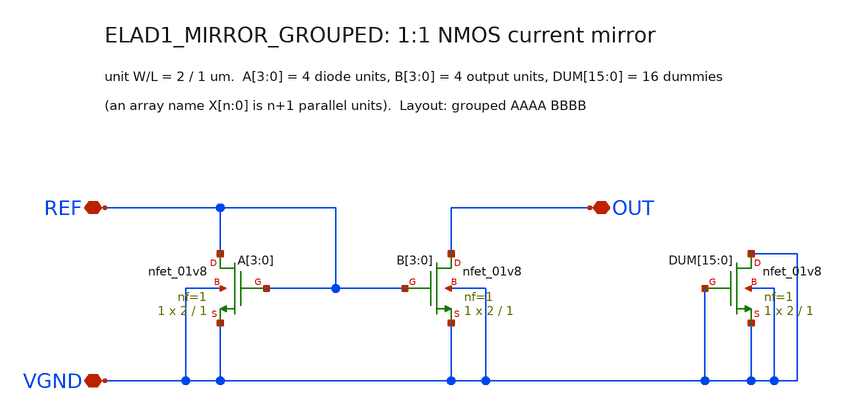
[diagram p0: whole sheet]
** sch_path: cells/ELAD1_MIRROR_GROUPED/schematic/ELAD1_MIRROR_GROUPED.sch
**.subckt ELAD1_MIRROR_GROUPED REF OUT VGND
*.iopin REF
*.iopin OUT
*.iopin VGND
XA[3] REF REF VGND VGND sky130_fd_pr__nfet_01v8 L=1 W=2 nf=1 ad='int((1 + 1)/2) * 2 / 1 * 0.29' as='int((1 + 2)/2) * 2 / 1 * 0.29'
+ pd='2*int((1 + 1)/2) * (2 / 1 + 0.29)' ps='2*int((1 + 2)/2) * (2 / 1 + 0.29)' nrd='0.29 / 2 ' nrs='0.29 / 2 '
+ sa=0 sb=0 sd=0 mult=1 m=1
XA[2] REF REF VGND VGND sky130_fd_pr__nfet_01v8 L=1 W=2 nf=1 ad='int((1 + 1)/2) * 2 / 1 * 0.29' as='int((1 + 2)/2) * 2 / 1 * 0.29'
+ pd='2*int((1 + 1)/2) * (2 / 1 + 0.29)' ps='2*int((1 + 2)/2) * (2 / 1 + 0.29)' nrd='0.29 / 2 ' nrs='0.29 / 2 '
+ sa=0 sb=0 sd=0 mult=1 m=1
XA[1] REF REF VGND VGND sky130_fd_pr__nfet_01v8 L=1 W=2 nf=1 ad='int((1 + 1)/2) * 2 / 1 * 0.29' as='int((1 + 2)/2) * 2 / 1 * 0.29'
+ pd='2*int((1 + 1)/2) * (2 / 1 + 0.29)' ps='2*int((1 + 2)/2) * (2 / 1 + 0.29)' nrd='0.29 / 2 ' nrs='0.29 / 2 '
+ sa=0 sb=0 sd=0 mult=1 m=1
XA[0] REF REF VGND VGND sky130_fd_pr__nfet_01v8 L=1 W=2 nf=1 ad='int((1 + 1)/2) * 2 / 1 * 0.29' as='int((1 + 2)/2) * 2 / 1 * 0.29'
+ pd='2*int((1 + 1)/2) * (2 / 1 + 0.29)' ps='2*int((1 + 2)/2) * (2 / 1 + 0.29)' nrd='0.29 / 2 ' nrs='0.29 / 2 '
+ sa=0 sb=0 sd=0 mult=1 m=1
XB[3] OUT REF VGND VGND sky130_fd_pr__nfet_01v8 L=1 W=2 nf=1 ad='int((1 + 1)/2) * 2 / 1 * 0.29' as='int((1 + 2)/2) * 2 / 1 * 0.29'
+ pd='2*int((1 + 1)/2) * (2 / 1 + 0.29)' ps='2*int((1 + 2)/2) * (2 / 1 + 0.29)' nrd='0.29 / 2 ' nrs='0.29 / 2 '
+ sa=0 sb=0 sd=0 mult=1 m=1
XB[2] OUT REF VGND VGND sky130_fd_pr__nfet_01v8 L=1 W=2 nf=1 ad='int((1 + 1)/2) * 2 / 1 * 0.29' as='int((1 + 2)/2) * 2 / 1 * 0.29'
+ pd='2*int((1 + 1)/2) * (2 / 1 + 0.29)' ps='2*int((1 + 2)/2) * (2 / 1 + 0.29)' nrd='0.29 / 2 ' nrs='0.29 / 2 '
+ sa=0 sb=0 sd=0 mult=1 m=1
XB[1] OUT REF VGND VGND sky130_fd_pr__nfet_01v8 L=1 W=2 nf=1 ad='int((1 + 1)/2) * 2 / 1 * 0.29' as='int((1 + 2)/2) * 2 / 1 * 0.29'
+ pd='2*int((1 + 1)/2) * (2 / 1 + 0.29)' ps='2*int((1 + 2)/2) * (2 / 1 + 0.29)' nrd='0.29 / 2 ' nrs='0.29 / 2 '
+ sa=0 sb=0 sd=0 mult=1 m=1
XB[0] OUT REF VGND VGND sky130_fd_pr__nfet_01v8 L=1 W=2 nf=1 ad='int((1 + 1)/2) * 2 / 1 * 0.29' as='int((1 + 2)/2) * 2 / 1 * 0.29'
+ pd='2*int((1 + 1)/2) * (2 / 1 + 0.29)' ps='2*int((1 + 2)/2) * (2 / 1 + 0.29)' nrd='0.29 / 2 ' nrs='0.29 / 2 '
+ sa=0 sb=0 sd=0 mult=1 m=1
XDUM[15] VGND VGND VGND VGND sky130_fd_pr__nfet_01v8 L=1 W=2 nf=1 ad='int((1 + 1)/2) * 2 / 1 * 0.29'
+ as='int((1 + 2)/2) * 2 / 1 * 0.29' pd='2*int((1 + 1)/2) * (2 / 1 + 0.29)' ps='2*int((1 + 2)/2) * (2 / 1 + 0.29)'
+ nrd='0.29 / 2 ' nrs='0.29 / 2 ' sa=0 sb=0 sd=0 mult=1 m=1
XDUM[14] VGND VGND VGND VGND sky130_fd_pr__nfet_01v8 L=1 W=2 nf=1 ad='int((1 + 1)/2) * 2 / 1 * 0.29'
+ as='int((1 + 2)/2) * 2 / 1 * 0.29' pd='2*int((1 + 1)/2) * (2 / 1 + 0.29)' ps='2*int((1 + 2)/2) * (2 / 1 + 0.29)'
+ nrd='0.29 / 2 ' nrs='0.29 / 2 ' sa=0 sb=0 sd=0 mult=1 m=1
XDUM[13] VGND VGND VGND VGND sky130_fd_pr__nfet_01v8 L=1 W=2 nf=1 ad='int((1 + 1)/2) * 2 / 1 * 0.29'
+ as='int((1 + 2)/2) * 2 / 1 * 0.29' pd='2*int((1 + 1)/2) * (2 / 1 + 0.29)' ps='2*int((1 + 2)/2) * (2 / 1 + 0.29)'
+ nrd='0.29 / 2 ' nrs='0.29 / 2 ' sa=0 sb=0 sd=0 mult=1 m=1
XDUM[12] VGND VGND VGND VGND sky130_fd_pr__nfet_01v8 L=1 W=2 nf=1 ad='int((1 + 1)/2) * 2 / 1 * 0.29'
+ as='int((1 + 2)/2) * 2 / 1 * 0.29' pd='2*int((1 + 1)/2) * (2 / 1 + 0.29)' ps='2*int((1 + 2)/2) * (2 / 1 + 0.29)'
+ nrd='0.29 / 2 ' nrs='0.29 / 2 ' sa=0 sb=0 sd=0 mult=1 m=1
XDUM[11] VGND VGND VGND VGND sky130_fd_pr__nfet_01v8 L=1 W=2 nf=1 ad='int((1 + 1)/2) * 2 / 1 * 0.29'
+ as='int((1 + 2)/2) * 2 / 1 * 0.29' pd='2*int((1 + 1)/2) * (2 / 1 + 0.29)' ps='2*int((1 + 2)/2) * (2 / 1 + 0.29)'
+ nrd='0.29 / 2 ' nrs='0.29 / 2 ' sa=0 sb=0 sd=0 mult=1 m=1
XDUM[10] VGND VGND VGND VGND sky130_fd_pr__nfet_01v8 L=1 W=2 nf=1 ad='int((1 + 1)/2) * 2 / 1 * 0.29'
+ as='int((1 + 2)/2) * 2 / 1 * 0.29' pd='2*int((1 + 1)/2) * (2 / 1 + 0.29)' ps='2*int((1 + 2)/2) * (2 / 1 + 0.29)'
+ nrd='0.29 / 2 ' nrs='0.29 / 2 ' sa=0 sb=0 sd=0 mult=1 m=1
XDUM[9] VGND VGND VGND VGND sky130_fd_pr__nfet_01v8 L=1 W=2 nf=1 ad='int((1 + 1)/2) * 2 / 1 * 0.29' as='int((1 + 2)/2) * 2 / 1 * 0.29'
+ pd='2*int((1 + 1)/2) * (2 / 1 + 0.29)' ps='2*int((1 + 2)/2) * (2 / 1 + 0.29)' nrd='0.29 / 2 ' nrs='0.29 / 2 '
+ sa=0 sb=0 sd=0 mult=1 m=1
XDUM[8] VGND VGND VGND VGND sky130_fd_pr__nfet_01v8 L=1 W=2 nf=1 ad='int((1 + 1)/2) * 2 / 1 * 0.29' as='int((1 + 2)/2) * 2 / 1 * 0.29'
+ pd='2*int((1 + 1)/2) * (2 / 1 + 0.29)' ps='2*int((1 + 2)/2) * (2 / 1 + 0.29)' nrd='0.29 / 2 ' nrs='0.29 / 2 '
+ sa=0 sb=0 sd=0 mult=1 m=1
XDUM[7] VGND VGND VGND VGND sky130_fd_pr__nfet_01v8 L=1 W=2 nf=1 ad='int((1 + 1)/2) * 2 / 1 * 0.29' as='int((1 + 2)/2) * 2 / 1 * 0.29'
+ pd='2*int((1 + 1)/2) * (2 / 1 + 0.29)' ps='2*int((1 + 2)/2) * (2 / 1 + 0.29)' nrd='0.29 / 2 ' nrs='0.29 / 2 '
+ sa=0 sb=0 sd=0 mult=1 m=1
XDUM[6] VGND VGND VGND VGND sky130_fd_pr__nfet_01v8 L=1 W=2 nf=1 ad='int((1 + 1)/2) * 2 / 1 * 0.29' as='int((1 + 2)/2) * 2 / 1 * 0.29'
+ pd='2*int((1 + 1)/2) * (2 / 1 + 0.29)' ps='2*int((1 + 2)/2) * (2 / 1 + 0.29)' nrd='0.29 / 2 ' nrs='0.29 / 2 '
+ sa=0 sb=0 sd=0 mult=1 m=1
XDUM[5] VGND VGND VGND VGND sky130_fd_pr__nfet_01v8 L=1 W=2 nf=1 ad='int((1 + 1)/2) * 2 / 1 * 0.29' as='int((1 + 2)/2) * 2 / 1 * 0.29'
+ pd='2*int((1 + 1)/2) * (2 / 1 + 0.29)' ps='2*int((1 + 2)/2) * (2 / 1 + 0.29)' nrd='0.29 / 2 ' nrs='0.29 / 2 '
+ sa=0 sb=0 sd=0 mult=1 m=1
XDUM[4] VGND VGND VGND VGND sky130_fd_pr__nfet_01v8 L=1 W=2 nf=1 ad='int((1 + 1)/2) * 2 / 1 * 0.29' as='int((1 + 2)/2) * 2 / 1 * 0.29'
+ pd='2*int((1 + 1)/2) * (2 / 1 + 0.29)' ps='2*int((1 + 2)/2) * (2 / 1 + 0.29)' nrd='0.29 / 2 ' nrs='0.29 / 2 '
+ sa=0 sb=0 sd=0 mult=1 m=1
XDUM[3] VGND VGND VGND VGND sky130_fd_pr__nfet_01v8 L=1 W=2 nf=1 ad='int((1 + 1)/2) * 2 / 1 * 0.29' as='int((1 + 2)/2) * 2 / 1 * 0.29'
+ pd='2*int((1 + 1)/2) * (2 / 1 + 0.29)' ps='2*int((1 + 2)/2) * (2 / 1 + 0.29)' nrd='0.29 / 2 ' nrs='0.29 / 2 '
+ sa=0 sb=0 sd=0 mult=1 m=1
XDUM[2] VGND VGND VGND VGND sky130_fd_pr__nfet_01v8 L=1 W=2 nf=1 ad='int((1 + 1)/2) * 2 / 1 * 0.29' as='int((1 + 2)/2) * 2 / 1 * 0.29'
+ pd='2*int((1 + 1)/2) * (2 / 1 + 0.29)' ps='2*int((1 + 2)/2) * (2 / 1 + 0.29)' nrd='0.29 / 2 ' nrs='0.29 / 2 '
+ sa=0 sb=0 sd=0 mult=1 m=1
XDUM[1] VGND VGND VGND VGND sky130_fd_pr__nfet_01v8 L=1 W=2 nf=1 ad='int((1 + 1)/2) * 2 / 1 * 0.29' as='int((1 + 2)/2) * 2 / 1 * 0.29'
+ pd='2*int((1 + 1)/2) * (2 / 1 + 0.29)' ps='2*int((1 + 2)/2) * (2 / 1 + 0.29)' nrd='0.29 / 2 ' nrs='0.29 / 2 '
+ sa=0 sb=0 sd=0 mult=1 m=1
XDUM[0] VGND VGND VGND VGND sky130_fd_pr__nfet_01v8 L=1 W=2 nf=1 ad='int((1 + 1)/2) * 2 / 1 * 0.29' as='int((1 + 2)/2) * 2 / 1 * 0.29'
+ pd='2*int((1 + 1)/2) * (2 / 1 + 0.29)' ps='2*int((1 + 2)/2) * (2 / 1 + 0.29)' nrd='0.29 / 2 ' nrs='0.29 / 2 '
+ sa=0 sb=0 sd=0 mult=1 m=1
**.ends
.end
